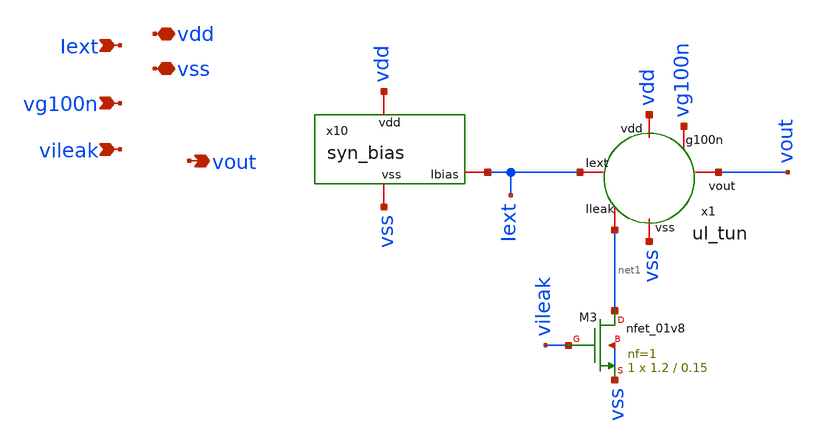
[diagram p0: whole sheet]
** sch_path: Neuron/ultralif/oneNeuron.sch
**.subckt oneNeuron vdd vss Iext vg100n vileak vout
*.iopin vdd
*.iopin vss
*.ipin Iext
*.ipin vg100n
*.ipin vileak
*.opin vout
x1 Iext vdd vg100n vout net1 vss ul_tun
XM3 net1 vileak vss vss sky130_fd_pr__nfet_01v8 L=0.15 W=1.2 nf=1 ad='int((nf+1)/2) * W/nf * 0.29' as='int((nf+2)/2) * W/nf * 0.29'
+ pd='2*int((nf+1)/2) * (W/nf + 0.29)' ps='2*int((nf+2)/2) * (W/nf + 0.29)' nrd='0.29 / W' nrs='0.29 / W'
+ sa=0 sb=0 sd=0 mult=1 m=1
x10 vdd vss Iext syn_bias
**.ends

* expanding   symbol:  Neuron/ultralif/ul_tun.sym # of pins=6
** sym_path: Neuron/ultralif/ul_tun.sym
** sch_path: Neuron/ultralif/ul_tun.sch
.subckt ul_tun Iext vdd g100n vout Ileak vss
*.iopin Iext
*.iopin vout
*.iopin vss
*.iopin Ileak
*.iopin vdd
*.iopin g100n
XM1 Ileak Ileak net1 vdd sky130_fd_pr__pfet_01v8 L=10 W=1 nf=1 ad='int((nf+1)/2) * W/nf * 0.29' as='int((nf+2)/2) * W/nf * 0.29'
+ pd='2*int((nf+1)/2) * (W/nf + 0.29)' ps='2*int((nf+2)/2) * (W/nf + 0.29)' nrd='0.29 / W' nrs='0.29 / W'
+ sa=0 sb=0 sd=0 mult=1 m=1
XM2 Ileak net2 net1 vdd sky130_fd_pr__pfet_01v8 L=0.15 W=1.5 nf=1 ad='int((nf+1)/2) * W/nf * 0.29' as='int((nf+2)/2) * W/nf * 0.29'
+ pd='2*int((nf+1)/2) * (W/nf + 0.29)' ps='2*int((nf+2)/2) * (W/nf + 0.29)' nrd='0.29 / W' nrs='0.29 / W'
+ sa=0 sb=0 sd=0 mult=1 m=1
XM3 net2 net2 net1 vdd sky130_fd_pr__pfet_01v8 L=0.15 W=15 nf=1 ad='int((nf+1)/2) * W/nf * 0.29' as='int((nf+2)/2) * W/nf * 0.29'
+ pd='2*int((nf+1)/2) * (W/nf + 0.29)' ps='2*int((nf+2)/2) * (W/nf + 0.29)' nrd='0.29 / W' nrs='0.29 / W'
+ sa=0 sb=0 sd=0 mult=1 m=1
XM4 net2 Ileak vss vss sky130_fd_pr__nfet_01v8 L=4 W=1 nf=1 ad='int((1 + 1)/2) * 1 / 1 * 0.29' as='int((1 + 2)/2) * 1 / 1 * 0.29'
+ pd='2*int((1 + 1)/2) * (1 / 1 + 0.29)' ps='2*int((1 + 2)/2) * (1 / 1 + 0.29)' nrd='0.29 / 1 ' nrs='0.29 / 1 '
+ sa=0 sb=0 sd=0 mult=1 m=1
C1 net1 vss 1p m=1
XM5 vout_n Ileak vss vss sky130_fd_pr__nfet_01v8 L=0.15 W=1 nf=1 ad='int((1 + 1)/2) * 1 / 1 * 0.29' as='int((1 + 2)/2) * 1 / 1 * 0.29'
+ pd='2*int((1 + 1)/2) * (1 / 1 + 0.29)' ps='2*int((1 + 2)/2) * (1 / 1 + 0.29)' nrd='0.29 / 1 ' nrs='0.29 / 1 '
+ sa=0 sb=0 sd=0 mult=1 m=1
XM6 vout_n g100n vdd vdd sky130_fd_pr__pfet_01v8 L=0.15 W=2 nf=1 ad='int((nf+1)/2) * W/nf * 0.29' as='int((nf+2)/2) * W/nf * 0.29'
+ pd='2*int((nf+1)/2) * (W/nf + 0.29)' ps='2*int((nf+2)/2) * (W/nf + 0.29)' nrd='0.29 / W' nrs='0.29 / W'
+ sa=0 sb=0 sd=0 mult=1 m=1
XM7 vout vout_n vss vss sky130_fd_pr__nfet_01v8 L=0.15 W=1 nf=1 ad='int((1 + 1)/2) * 1 / 1 * 0.29' as='int((1 + 2)/2) * 1 / 1 * 0.29'
+ pd='2*int((1 + 1)/2) * (1 / 1 + 0.29)' ps='2*int((1 + 2)/2) * (1 / 1 + 0.29)' nrd='0.29 / 1 ' nrs='0.29 / 1 '
+ sa=0 sb=0 sd=0 mult=1 m=1
XM8 vout vout_n vdd vdd sky130_fd_pr__pfet_01v8 L=0.15 W=2 nf=1 ad='int((nf+1)/2) * W/nf * 0.29' as='int((nf+2)/2) * W/nf * 0.29'
+ pd='2*int((nf+1)/2) * (W/nf + 0.29)' ps='2*int((nf+2)/2) * (W/nf + 0.29)' nrd='0.29 / W' nrs='0.29 / W'
+ sa=0 sb=0 sd=0 mult=1 m=1
vext Iext net1 0
**** begin user architecture code


.save i(vext)


**** end user architecture code
.ends


* expanding   symbol:  /home/alex/Desktop/EDA/SNN_IPN/Neuron/ultralif/syn_bias.sym # of pins=3
** sym_path: Neuron/ultralif/syn_bias.sym
** sch_path: Neuron/ultralif/syn_bias.sch
.subckt syn_bias vdd vss Ibias
*.iopin vss
*.iopin vdd
*.iopin Ibias
XM2 Ibias net1 vdd vdd sky130_fd_pr__pfet_01v8 L=1 W=0.5 nf=1 ad='int((nf+1)/2) * W/nf * 0.29' as='int((nf+2)/2) * W/nf * 0.29'
+ pd='2*int((nf+1)/2) * (W/nf + 0.29)' ps='2*int((nf+2)/2) * (W/nf + 0.29)' nrd='0.29 / W' nrs='0.29 / W'
+ sa=0 sb=0 sd=0 mult=1 m=1
XR1 net1 vdd sky130_fd_pr__res_generic_po W=1.15 L=1 m=1
XR2 vss net1 sky130_fd_pr__res_generic_po W=1 L=1 m=1
.ends

.end
